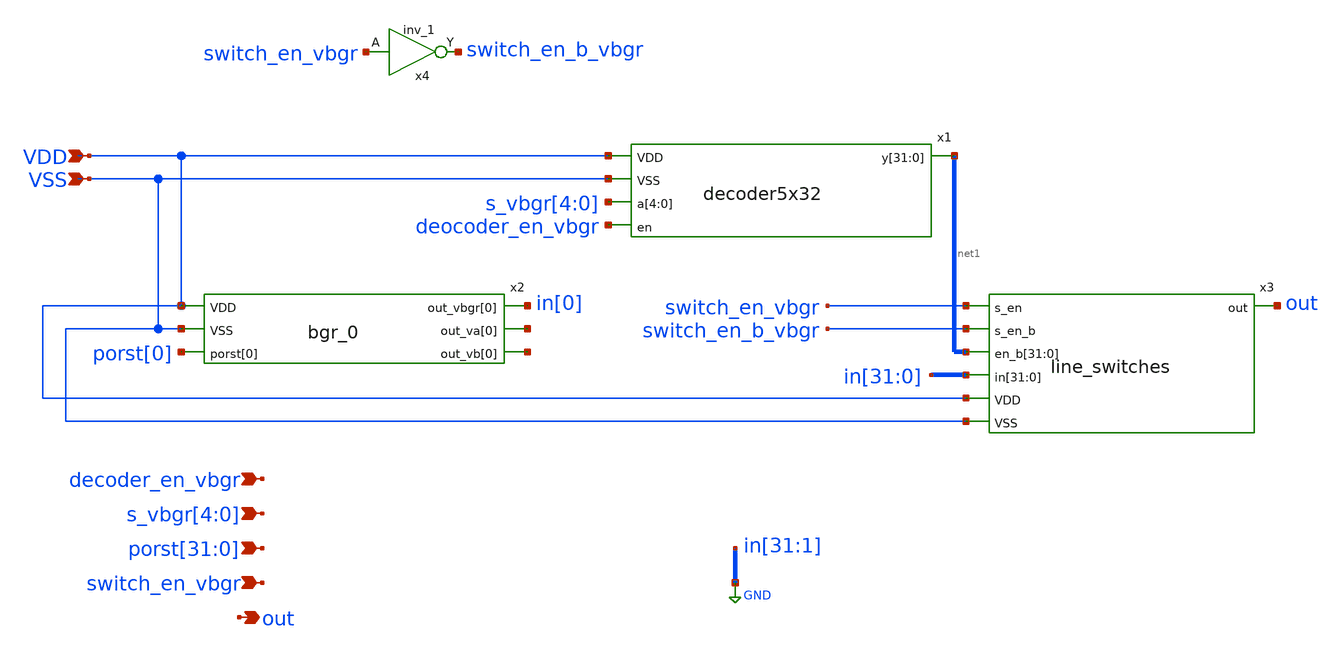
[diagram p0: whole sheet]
** sch_path: final_top/schematic/final_macro.sch
**.subckt final_macro VDD VSS
*+ porst[31],porst[30],porst[29],porst[28],porst[27],porst[26],porst[25],porst[24],porst[23],porst[22],porst[21],porst[20],porst[19],porst[18],porst[17],porst[16],porst[15],porst[14],porst[13],porst[12],porst[11],porst[10],porst[9],porst[8],porst[7],porst[6],porst[5],porst[4],porst[3],porst[2],porst[1],porst[0] s_vbgr[4],s_vbgr[3],s_vbgr[2],s_vbgr[1],s_vbgr[0] decoder_en_vbgr switch_en_vbgr out
*.ipin VDD
*.ipin VSS
*.ipin
*+ porst[31],porst[30],porst[29],porst[28],porst[27],porst[26],porst[25],porst[24],porst[23],porst[22],porst[21],porst[20],porst[19],porst[18],porst[17],porst[16],porst[15],porst[14],porst[13],porst[12],porst[11],porst[10],porst[9],porst[8],porst[7],porst[6],porst[5],porst[4],porst[3],porst[2],porst[1],porst[0]
*.ipin s_vbgr[4],s_vbgr[3],s_vbgr[2],s_vbgr[1],s_vbgr[0]
*.ipin decoder_en_vbgr
*.ipin switch_en_vbgr
*.opin out
x2 VDD VSS porst[0] in[0] net2 net3 bgr_0
x4 switch_en_vbgr VGND VNB VPB VPWR switch_en_b_vbgr sky130_fd_sc_hd__inv_1
x1 VDD VSS s_vbgr[4] s_vbgr[3] s_vbgr[2] s_vbgr[1] s_vbgr[0] deocoder_en_vbgr net1[31] net1[30]
+ net1[29] net1[28] net1[27] net1[26] net1[25] net1[24] net1[23] net1[22] net1[21] net1[20] net1[19] net1[18]
+ net1[17] net1[16] net1[15] net1[14] net1[13] net1[12] net1[11] net1[10] net1[9] net1[8] net1[7] net1[6]
+ net1[5] net1[4] net1[3] net1[2] net1[1] net1[0] decoder5x32
x3 switch_en_vbgr switch_en_b_vbgr out net1[31] net1[30] net1[29] net1[28] net1[27] net1[26]
+ net1[25] net1[24] net1[23] net1[22] net1[21] net1[20] net1[19] net1[18] net1[17] net1[16] net1[15] net1[14]
+ net1[13] net1[12] net1[11] net1[10] net1[9] net1[8] net1[7] net1[6] net1[5] net1[4] net1[3] net1[2] net1[1]
+ net1[0] in[31] in[30] in[29] in[28] in[27] in[26] in[25] in[24] in[23] in[22] in[21] in[20] in[19] in[18]
+ in[17] in[16] in[15] in[14] in[13] in[12] in[11] in[10] in[9] in[8] in[7] in[6] in[5] in[4] in[3] in[2]
+ in[1] in[0] VDD VSS line_switches
**.ends
.GLOBAL GND
.end
